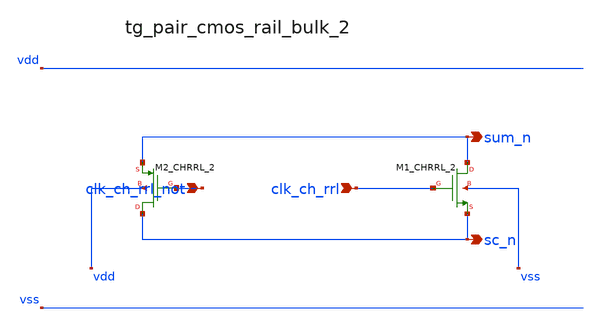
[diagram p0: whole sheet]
** sch_path: analog-db/raw/sup_003_rrl_sc_integrator/hier/blocks/tg_pair_cmos_rail_bulk_2.sch
**.subckt tg_pair_cmos_rail_bulk_2 clk_ch_rrl_not clk_ch_rrl sum_n sc_n
*.ipin clk_ch_rrl_not
*.ipin clk_ch_rrl
*.opin sum_n
*.opin sc_n
XM1_CHRRL_2 sum_n clk_ch_rrl sc_n vss sg13_lv_nmos w=x_dut_xm1_chrrl_2_w l=x_dut_xm1_chrrl_2_l ng=1
+ m=x_dut_xm1_chrrl_2_m
XM2_CHRRL_2 sc_n clk_ch_rrl_not sum_n vdd sg13_lv_pmos w=x_dut_xm2_chrrl_2_w l=x_dut_xm2_chrrl_2_l
+ ng=1 m=x_dut_xm2_chrrl_2_m
**.ends
.end
